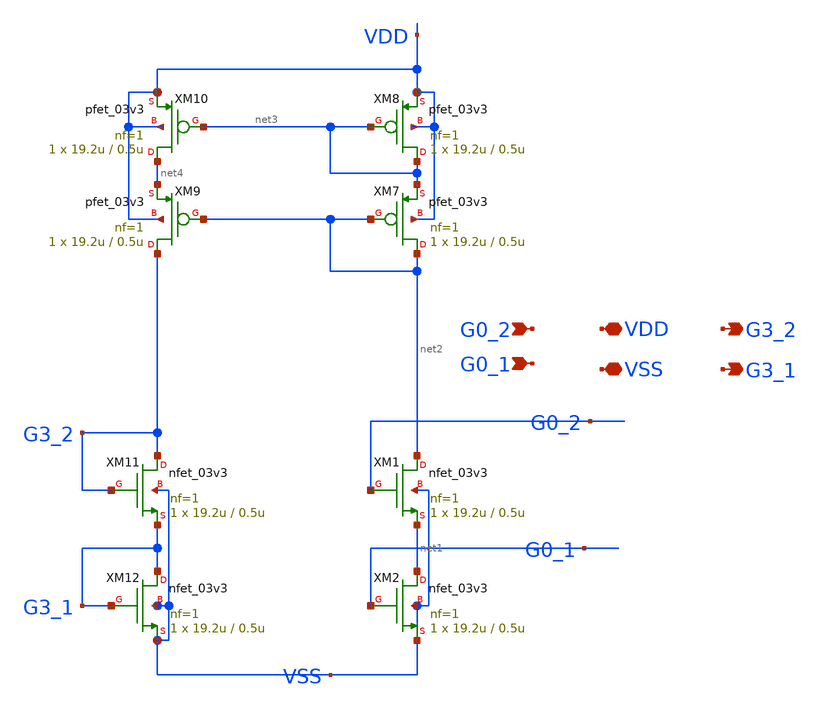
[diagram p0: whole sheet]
** sch_path: DAC_PAKISTAN_01/Pakistan1_Xschem/CM_32_s.sch
**.subckt CM_32_s G0_2 VDD VSS G3_2 G0_1 G3_1
*.ipin G0_2
*.iopin VDD
*.iopin VSS
*.opin G3_2
*.ipin G0_1
*.opin G3_1
XM1 net2 G0_2 net1 VSS nfet_03v3 L=0.5u W=19.2u nf=1 ad='int((nf+1)/2) * W/nf * 0.18u' as='int((nf+2)/2) * W/nf * 0.18u'
+ pd='2*int((nf+1)/2) * (W/nf + 0.18u)' ps='2*int((nf+2)/2) * (W/nf + 0.18u)' nrd='0.18u / W' nrs='0.18u / W'
+ sa=0 sb=0 sd=0 m=1
XM2 net1 G0_1 VSS VSS nfet_03v3 L=0.5u W=19.2u nf=1 ad='int((nf+1)/2) * W/nf * 0.18u' as='int((nf+2)/2) * W/nf * 0.18u'
+ pd='2*int((nf+1)/2) * (W/nf + 0.18u)' ps='2*int((nf+2)/2) * (W/nf + 0.18u)' nrd='0.18u / W' nrs='0.18u / W'
+ sa=0 sb=0 sd=0 m=1
XM7 net2 net2 net3 VDD pfet_03v3 L=0.5u W=19.2u nf=1 ad='int((nf+1)/2) * W/nf * 0.18u' as='int((nf+2)/2) * W/nf * 0.18u'
+ pd='2*int((nf+1)/2) * (W/nf + 0.18u)' ps='2*int((nf+2)/2) * (W/nf + 0.18u)' nrd='0.18u / W' nrs='0.18u / W'
+ sa=0 sb=0 sd=0 m=1
XM8 net3 net3 VDD VDD pfet_03v3 L=0.5u W=19.2u nf=1 ad='int((nf+1)/2) * W/nf * 0.18u' as='int((nf+2)/2) * W/nf * 0.18u'
+ pd='2*int((nf+1)/2) * (W/nf + 0.18u)' ps='2*int((nf+2)/2) * (W/nf + 0.18u)' nrd='0.18u / W' nrs='0.18u / W'
+ sa=0 sb=0 sd=0 m=1
XM9 G3_2 net2 net4 VDD pfet_03v3 L=0.5u W=19.2u nf=1 ad='int((nf+1)/2) * W/nf * 0.18u' as='int((nf+2)/2) * W/nf * 0.18u'
+ pd='2*int((nf+1)/2) * (W/nf + 0.18u)' ps='2*int((nf+2)/2) * (W/nf + 0.18u)' nrd='0.18u / W' nrs='0.18u / W'
+ sa=0 sb=0 sd=0 m=1
XM10 net4 net3 VDD VDD pfet_03v3 L=0.5u W=19.2u nf=1 ad='int((nf+1)/2) * W/nf * 0.18u' as='int((nf+2)/2) * W/nf * 0.18u'
+ pd='2*int((nf+1)/2) * (W/nf + 0.18u)' ps='2*int((nf+2)/2) * (W/nf + 0.18u)' nrd='0.18u / W' nrs='0.18u / W'
+ sa=0 sb=0 sd=0 m=1
XM11 G3_2 G3_2 G3_1 VSS nfet_03v3 L=0.5u W=19.2u nf=1 ad='int((nf+1)/2) * W/nf * 0.18u' as='int((nf+2)/2) * W/nf * 0.18u'
+ pd='2*int((nf+1)/2) * (W/nf + 0.18u)' ps='2*int((nf+2)/2) * (W/nf + 0.18u)' nrd='0.18u / W' nrs='0.18u / W'
+ sa=0 sb=0 sd=0 m=1
XM12 G3_1 G3_1 VSS VSS nfet_03v3 L=0.5u W=19.2u nf=1 ad='int((nf+1)/2) * W/nf * 0.18u' as='int((nf+2)/2) * W/nf * 0.18u'
+ pd='2*int((nf+1)/2) * (W/nf + 0.18u)' ps='2*int((nf+2)/2) * (W/nf + 0.18u)' nrd='0.18u / W' nrs='0.18u / W'
+ sa=0 sb=0 sd=0 m=1
**.ends
.end
